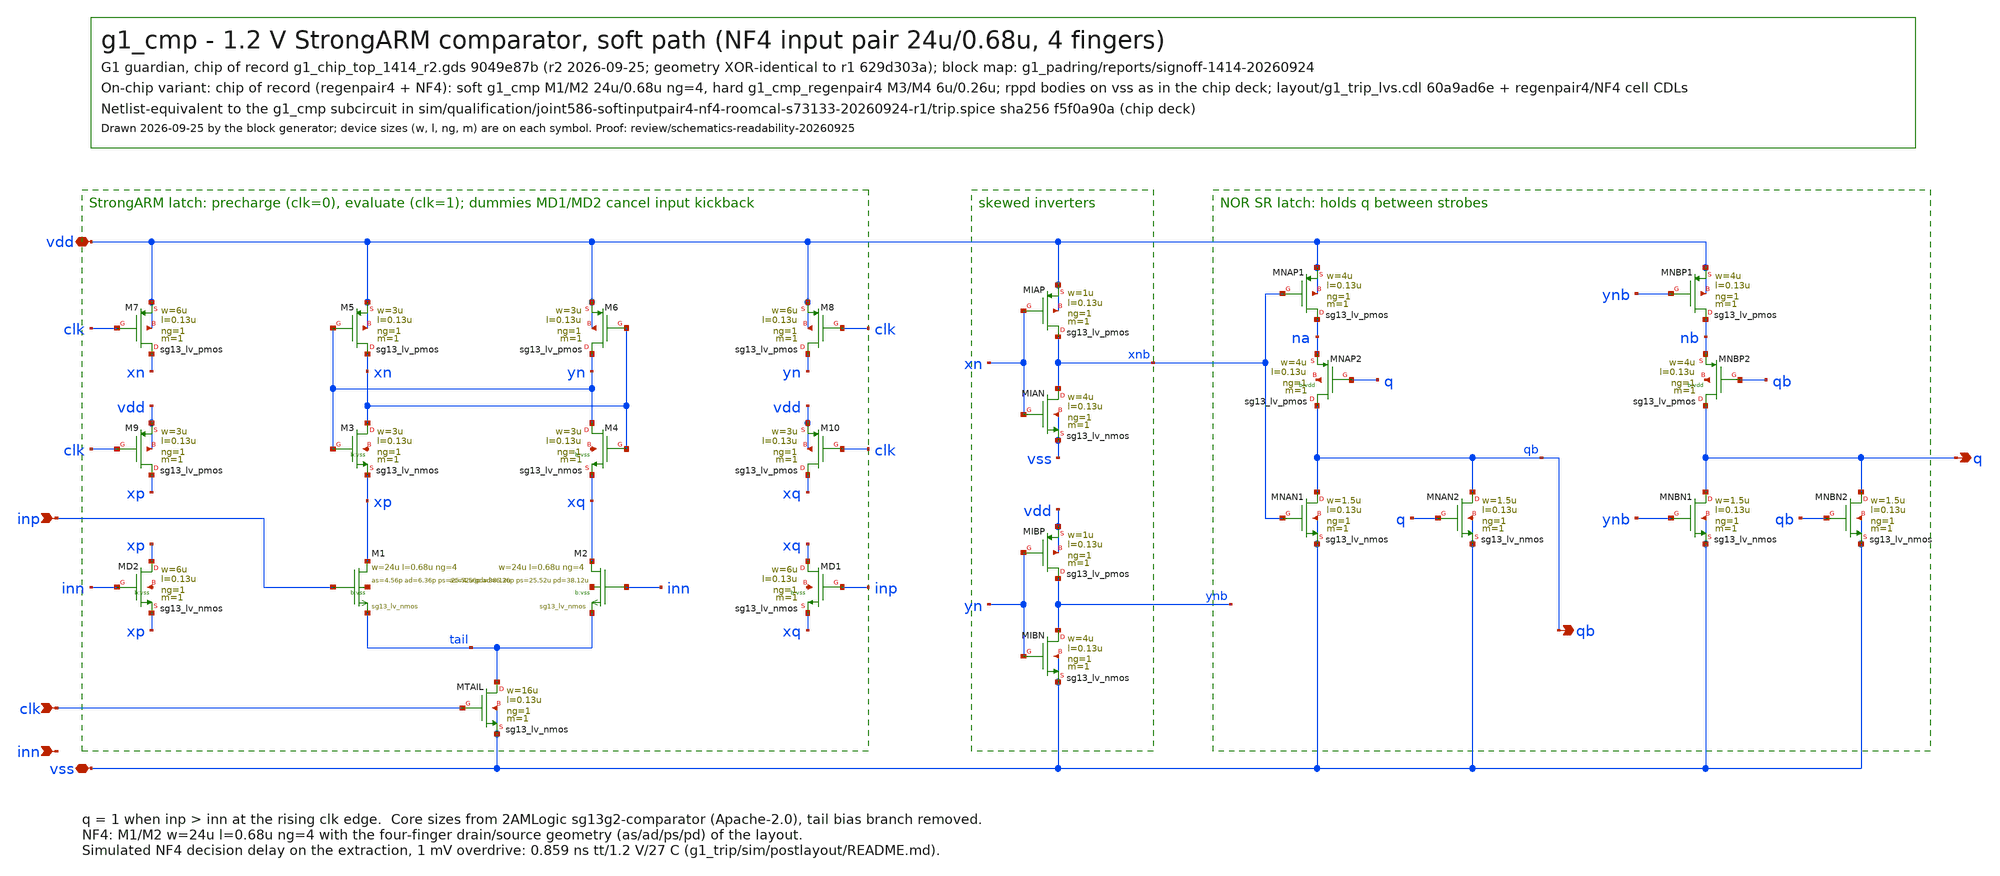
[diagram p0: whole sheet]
** sch_path: designs/g1-guardian/blocks/g1_trip/schematic/g1_cmp.sch
**.subckt g1_cmp inp inn clk q qb vdd vss
*.ipin inp
*.ipin inn
*.ipin clk
*.opin q
*.opin qb
*.iopin vdd
*.iopin vss
XMTAIL tail clk vss vss sg13_lv_nmos w=16u l=0.13u ng=1 m=1 mm_ok=1
XM1 xp inp tail vss sg13_lv_nmos w=24u l=0.68u ng=4 m=1 mm_ok=1 as=4.56p ad=6.36p ps=25.52u
+ pd=38.12u
XM2 xq inn tail vss sg13_lv_nmos w=24u l=0.68u ng=4 m=1 mm_ok=1 as=4.56p ad=6.36p ps=25.52u
+ pd=38.12u
XMD1 xq inp xq vss sg13_lv_nmos w=6u l=0.13u ng=1 m=1 mm_ok=1
XMD2 xp inn xp vss sg13_lv_nmos w=6u l=0.13u ng=1 m=1 mm_ok=1
XM3 xn yn xp vss sg13_lv_nmos w=3u l=0.13u ng=1 m=1 mm_ok=1
XM4 yn xn xq vss sg13_lv_nmos w=3u l=0.13u ng=1 m=1 mm_ok=1
XM5 xn yn vdd vdd sg13_lv_pmos w=3u l=0.13u ng=1 m=1 mm_ok=1
XM6 yn xn vdd vdd sg13_lv_pmos w=3u l=0.13u ng=1 m=1 mm_ok=1
XM7 xn clk vdd vdd sg13_lv_pmos w=6u l=0.13u ng=1 m=1 mm_ok=1
XM8 yn clk vdd vdd sg13_lv_pmos w=6u l=0.13u ng=1 m=1 mm_ok=1
XM9 xp clk vdd vdd sg13_lv_pmos w=3u l=0.13u ng=1 m=1 mm_ok=1
XM10 xq clk vdd vdd sg13_lv_pmos w=3u l=0.13u ng=1 m=1 mm_ok=1
XMIAP xnb xn vdd vdd sg13_lv_pmos w=1u l=0.13u ng=1 m=1 mm_ok=1
XMIAN xnb xn vss vss sg13_lv_nmos w=4u l=0.13u ng=1 m=1 mm_ok=1
XMIBP ynb yn vdd vdd sg13_lv_pmos w=1u l=0.13u ng=1 m=1 mm_ok=1
XMIBN ynb yn vss vss sg13_lv_nmos w=4u l=0.13u ng=1 m=1 mm_ok=1
XMNAP1 na xnb vdd vdd sg13_lv_pmos w=4u l=0.13u ng=1 m=1 mm_ok=1
XMNAP2 qb q na vdd sg13_lv_pmos w=4u l=0.13u ng=1 m=1 mm_ok=1
XMNAN1 qb xnb vss vss sg13_lv_nmos w=1.5u l=0.13u ng=1 m=1 mm_ok=1
XMNAN2 qb q vss vss sg13_lv_nmos w=1.5u l=0.13u ng=1 m=1 mm_ok=1
XMNBP1 nb ynb vdd vdd sg13_lv_pmos w=4u l=0.13u ng=1 m=1 mm_ok=1
XMNBP2 q qb nb vdd sg13_lv_pmos w=4u l=0.13u ng=1 m=1 mm_ok=1
XMNBN1 q ynb vss vss sg13_lv_nmos w=1.5u l=0.13u ng=1 m=1 mm_ok=1
XMNBN2 q qb vss vss sg13_lv_nmos w=1.5u l=0.13u ng=1 m=1 mm_ok=1
**.ends
.end
